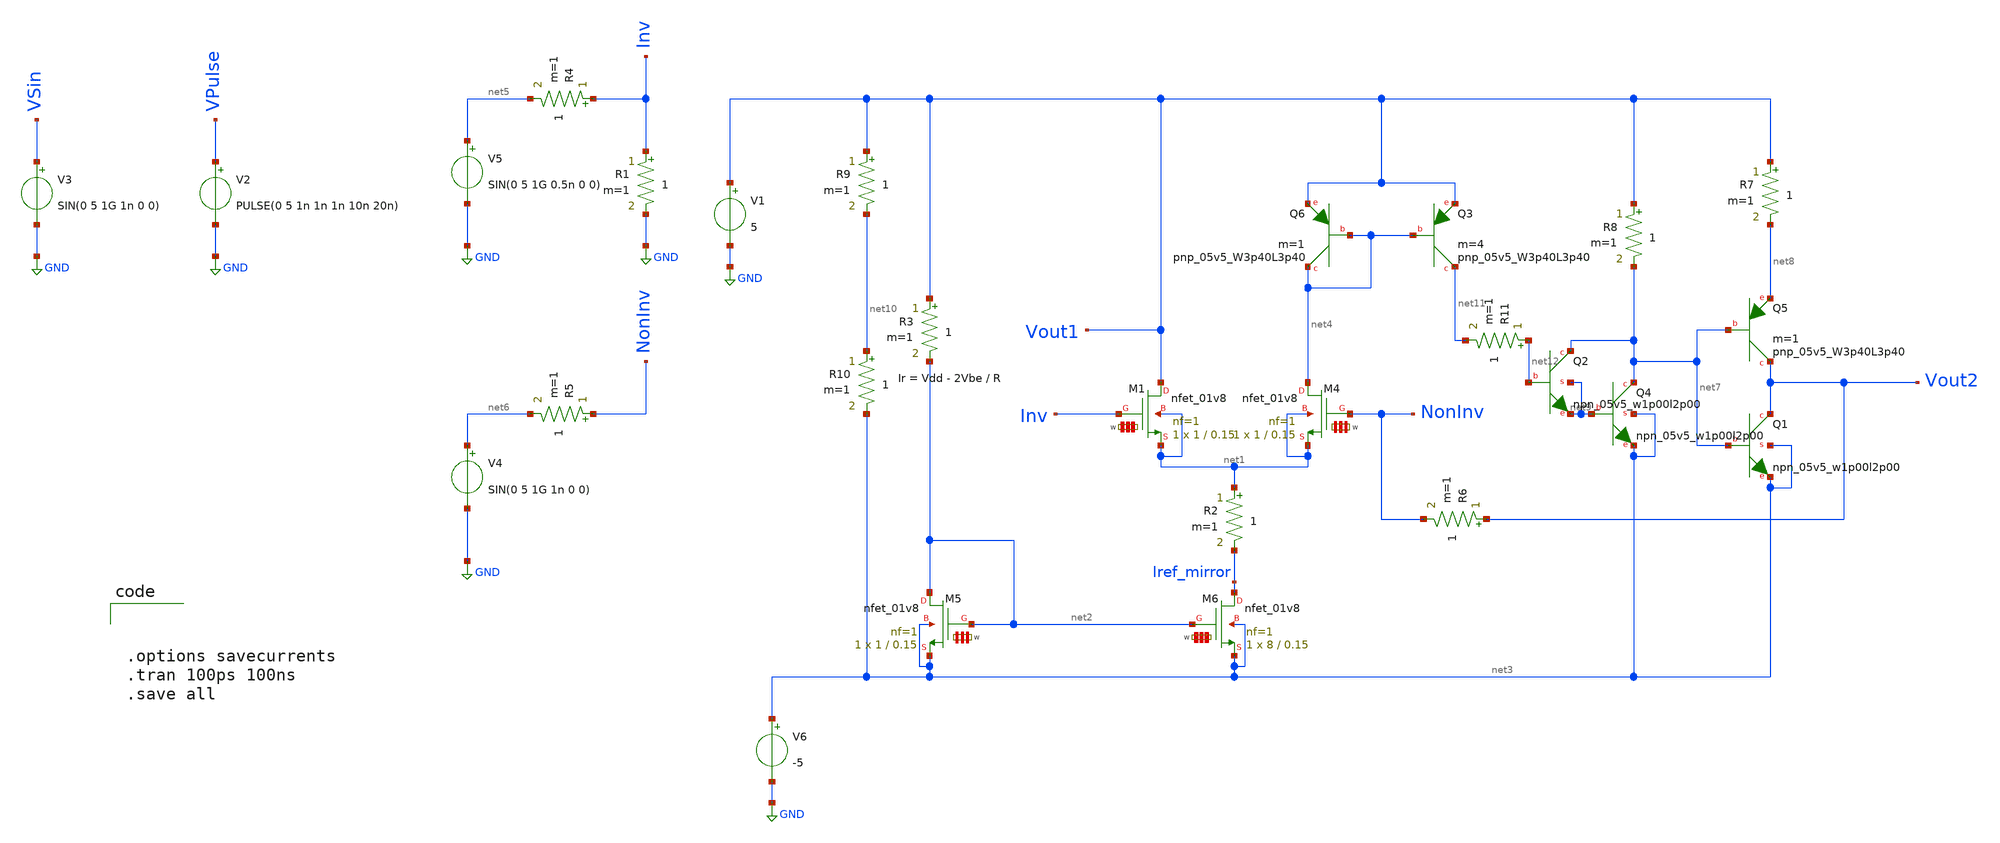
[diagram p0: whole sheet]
** sch_path: Sky130 xsch magic/xscheme/differential_amp.sch
**.subckt differential_amp
XM1 Vout1 Inv net1 net1 sky130_fd_pr__nfet_01v8 L=0.15 W='1 * 1 ' nf=1 ad='int((nf+1)/2) * W / nf * 0.29'
+ as='int((nf+2)/2) * W / nf * 0.29' pd='2*int((nf+1)/2) * (W / nf + 0.29)' ps='2*int((nf+2)/2) * (W / nf + 0.29)'
+ nrd='0.29 / W ' nrs='0.29 / W ' sa=0 sb=0 sd=0 mult=1 m=1
XM6 Iref_mirror net2 net3 net3 sky130_fd_pr__nfet_01v8 L=0.15 W='8 * 1 ' nf=1 ad='int((nf+1)/2) * W / nf * 0.29'
+ as='int((nf+2)/2) * W / nf * 0.29' pd='2*int((nf+1)/2) * (W / nf + 0.29)' ps='2*int((nf+2)/2) * (W / nf + 0.29)'
+ nrd='0.29 / W ' nrs='0.29 / W ' sa=0 sb=0 sd=0 mult=1 m=1
V2 VPulse GND PULSE(0 5 1n 1n 1n 10n 20n)
V3 VSin GND SIN(0 5 1G 1n 0 0)
XM5 net2 net2 net3 net3 sky130_fd_pr__nfet_01v8 L=0.15 W='1 * 1 ' nf=1 ad='int((nf+1)/2) * W / nf * 0.29'
+ as='int((nf+2)/2) * W / nf * 0.29' pd='2*int((nf+1)/2) * (W / nf + 0.29)' ps='2*int((nf+2)/2) * (W / nf + 0.29)'
+ nrd='0.29 / W ' nrs='0.29 / W ' sa=0 sb=0 sd=0 mult=1 m=1
XM4 net4 NonInv net1 net1 sky130_fd_pr__nfet_01v8 L=0.15 W='1 * 1 ' nf=1 ad='int((nf+1)/2) * W / nf * 0.29'
+ as='int((nf+2)/2) * W / nf * 0.29' pd='2*int((nf+1)/2) * (W / nf + 0.29)' ps='2*int((nf+2)/2) * (W / nf + 0.29)'
+ nrd='0.29 / W ' nrs='0.29 / W ' sa=0 sb=0 sd=0 mult=1 m=1
V4 net6 GND SIN(0 5 1G 1n 0 0)
V5 net5 GND SIN(0 5 1G 0.5n 0 0)
R3 Vout1 net2 1 m=1
R1 Inv GND 1 m=1
R4 Inv net5 1 m=1
R5 NonInv net6 1 m=1
R6 Vout2 NonInv 1 m=1
R7 Vout1 net8 1 m=1
XQ1 Vout2 net7 net3 net3 sky130_fd_pr__npn_05v5_w1p00l2p00
R2 net1 Iref_mirror 1 m=1
XQ3 net11 net4 Vout1 sky130_fd_pr__pnp_05v5_W3p40L3p40 m=4
XQ5 Vout2 net7 net8 sky130_fd_pr__pnp_05v5_W3p40L3p40 m=1
XQ6 net4 net4 Vout1 sky130_fd_pr__pnp_05v5_W3p40L3p40 m=1
XQ2 net7 net12 net9 net9 sky130_fd_pr__npn_05v5_w1p00l2p00
XQ4 net7 net9 net3 net3 sky130_fd_pr__npn_05v5_w1p00l2p00
R8 Vout1 net7 1 m=1
R9 Vout1 net10 1 m=1
R10 net10 net3 1 m=1
R11 net12 net11 1 m=1
V6 net3 GND -5
V1 Vout1 GND 5
**** begin user architecture code



.lib /usr/local/share/xschem/xschem_library/devices/sky130A/libs.tech/ngspice/sky130.lib.spice tt




.options savecurrents
.tran 100ps 100ns
.save all



**** end user architecture code
**.ends
.GLOBAL GND
.end
